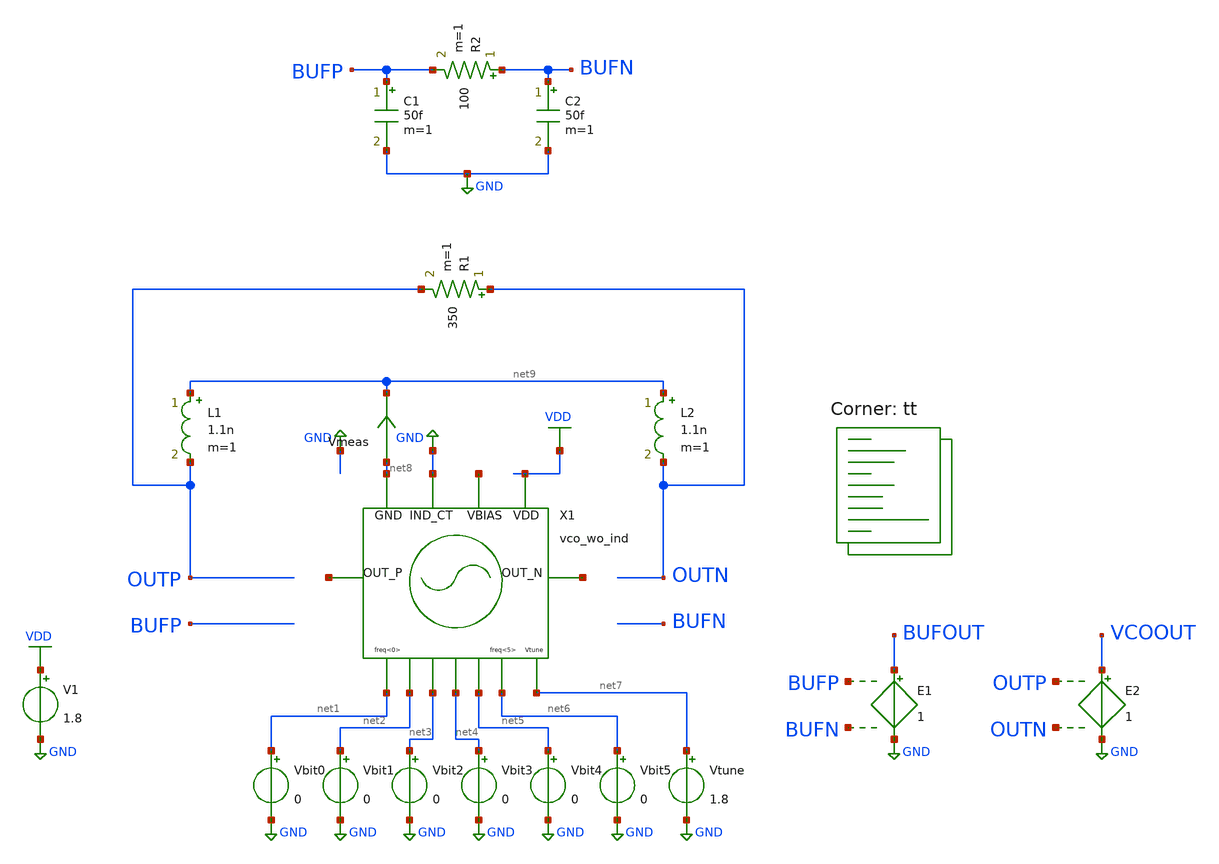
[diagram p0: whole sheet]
** sch_path: xschem/vco/testbenches/top/vco_wo_ind_sweep.sch
**.subckt vco_wo_ind_sweep
V1 VDD GND 1.8
Vbit0 net1 GND 0
Vbit1 net2 GND 0
Vbit2 net3 GND 0
Vbit3 net4 GND 0
Vbit4 net5 GND 0
Vbit5 net6 GND 0
L1 net9 OUTP 1.1n m=1
L2 net9 OUTN 1.1n m=1
Vtune net7 GND 1.8
R1 OUTN OUTP 350 m=1
R2 BUFN BUFP 100 m=1
C1 BUFP GND 50f m=1
C2 BUFN GND 50f m=1
E1 BUFOUT GND BUFP BUFN 1
E2 VCOOUT GND OUTP OUTN 1
X1 net10 net8 GND VDD net11 net1 net2 net3 net4 net5 net6 net12 net7 vco_wo_ind
Vmeas net8 net9 0
.save i(vmeas)
**** begin user architecture code
.lib $::SKYWATER_MODELS/sky130.lib.spice tt

.save

**** end user architecture code
**.ends
.GLOBAL GND
.GLOBAL VDD
.end
